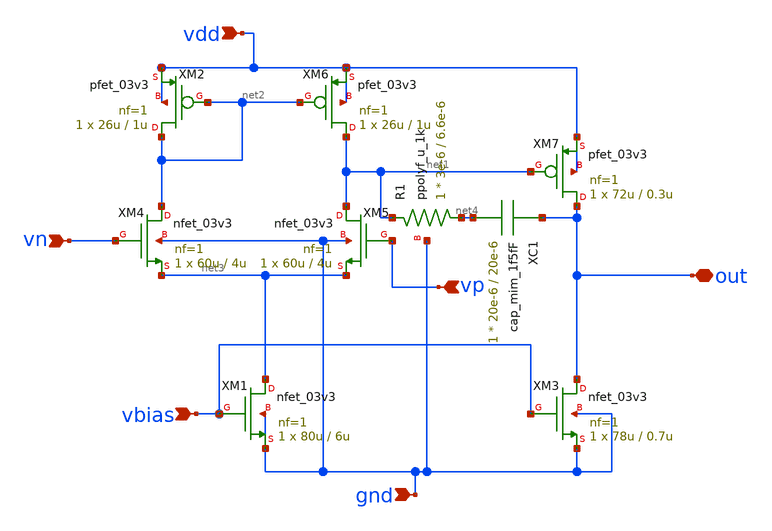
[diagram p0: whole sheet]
** sch_path: xschem/opamp/opamp.sch
**.subckt opamp gnd out vbias vp vn vdd
*.ipin gnd
*.iopin out
*.ipin vbias
*.ipin vp
*.ipin vn
*.ipin vdd
XM1 net3 vbias gnd gnd nfet_03v3 L=6u W=80u nf=1 ad='int((nf+1)/2) * W/nf * 0.18u' as='int((nf+2)/2) * W/nf * 0.18u'
+ pd='2*int((nf+1)/2) * (W/nf + 0.18u)' ps='2*int((nf+2)/2) * (W/nf + 0.18u)' nrd='0.18u / W' nrs='0.18u / W'
+ sa=0 sb=0 sd=0 m=1
XM2 net2 net2 vdd vdd pfet_03v3 L=1u W=26u nf=1 ad='int((nf+1)/2) * W/nf * 0.18u' as='int((nf+2)/2) * W/nf * 0.18u'
+ pd='2*int((nf+1)/2) * (W/nf + 0.18u)' ps='2*int((nf+2)/2) * (W/nf + 0.18u)' nrd='0.18u / W' nrs='0.18u / W'
+ sa=0 sb=0 sd=0 m=1
XM3 out vbias gnd gnd nfet_03v3 L=0.7u W=78u nf=1 ad='int((nf+1)/2) * W/nf * 0.18u' as='int((nf+2)/2) * W/nf * 0.18u'
+ pd='2*int((nf+1)/2) * (W/nf + 0.18u)' ps='2*int((nf+2)/2) * (W/nf + 0.18u)' nrd='0.18u / W' nrs='0.18u / W'
+ sa=0 sb=0 sd=0 m=1
XM4 net2 vn net3 gnd nfet_03v3 L=4u W=60u nf=1 ad='int((nf+1)/2) * W/nf * 0.18u' as='int((nf+2)/2) * W/nf * 0.18u'
+ pd='2*int((nf+1)/2) * (W/nf + 0.18u)' ps='2*int((nf+2)/2) * (W/nf + 0.18u)' nrd='0.18u / W' nrs='0.18u / W'
+ sa=0 sb=0 sd=0 m=1
XM5 net1 vp net3 gnd nfet_03v3 L=4u W=60u nf=1 ad='int((nf+1)/2) * W/nf * 0.18u' as='int((nf+2)/2) * W/nf * 0.18u'
+ pd='2*int((nf+1)/2) * (W/nf + 0.18u)' ps='2*int((nf+2)/2) * (W/nf + 0.18u)' nrd='0.18u / W' nrs='0.18u / W'
+ sa=0 sb=0 sd=0 m=1
XM6 net1 net2 vdd vdd pfet_03v3 L=1u W=26u nf=1 ad='int((nf+1)/2) * W/nf * 0.18u' as='int((nf+2)/2) * W/nf * 0.18u'
+ pd='2*int((nf+1)/2) * (W/nf + 0.18u)' ps='2*int((nf+2)/2) * (W/nf + 0.18u)' nrd='0.18u / W' nrs='0.18u / W'
+ sa=0 sb=0 sd=0 m=1
XM7 out net1 vdd vdd pfet_03v3 L=0.3u W=72u nf=1 ad='int((nf+1)/2) * W/nf * 0.18u' as='int((nf+2)/2) * W/nf * 0.18u'
+ pd='2*int((nf+1)/2) * (W/nf + 0.18u)' ps='2*int((nf+2)/2) * (W/nf + 0.18u)' nrd='0.18u / W' nrs='0.18u / W'
+ sa=0 sb=0 sd=0 m=1
XR1 net4 net1 gnd ppolyf_u_1k r_width=3e-6 r_length=6.6e-6 m=1
XC1 out net4 cap_mim_1f5fF c_width=20e-6 c_length=20e-6 m=1
**.ends
.end
